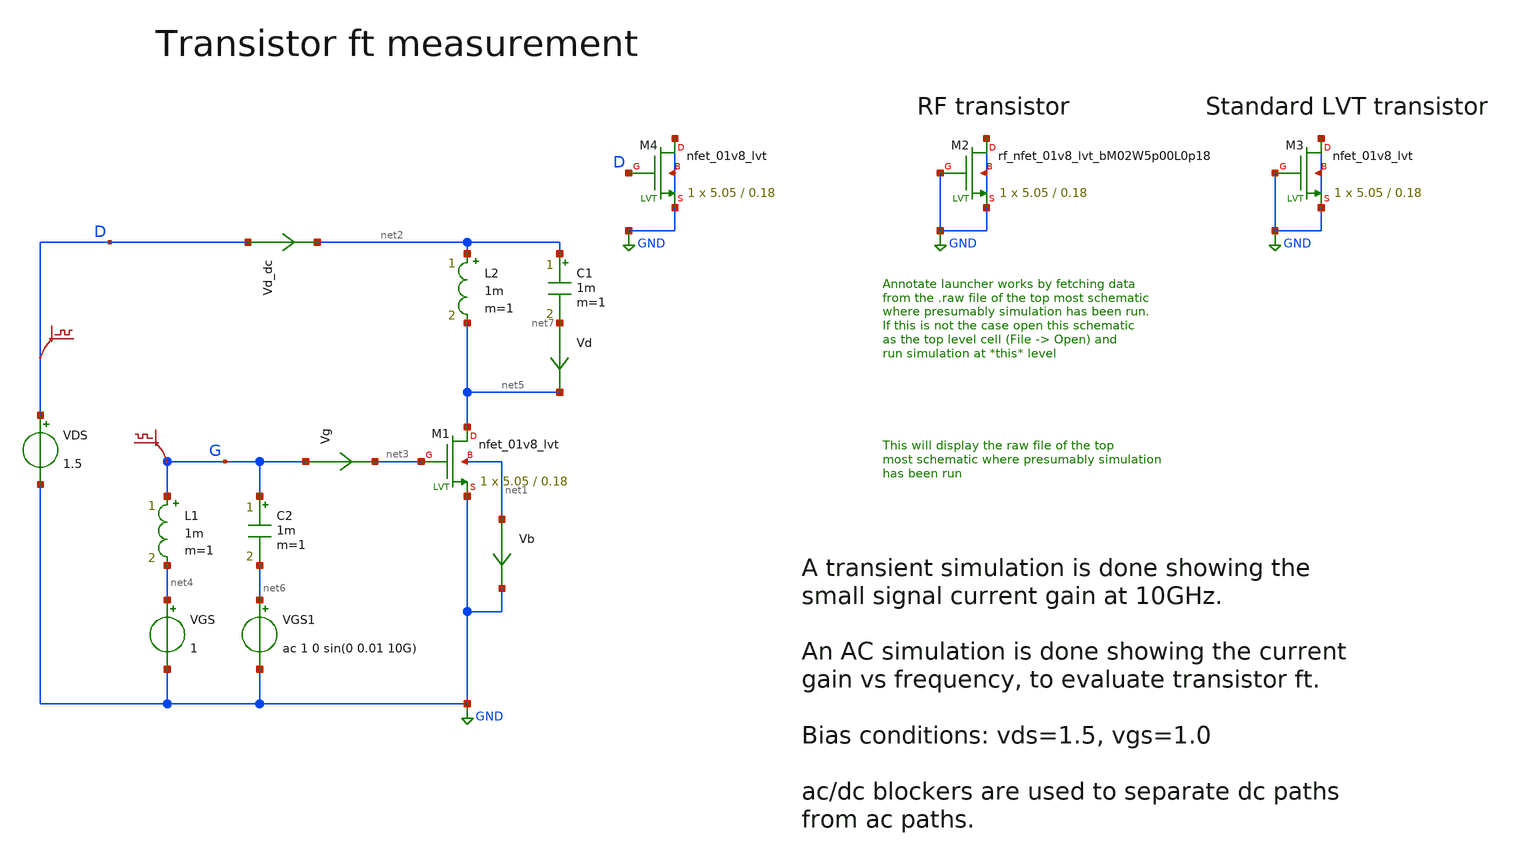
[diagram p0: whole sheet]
** sch_path: xyce/sky130A-xyce/libs.tech/xschem/sky130_tests/tb_ft_test_2.sch
**.subckt tb_ft_test_2
VDS D GND 1.5
VGS net4 GND 1
Vd net7 net5 0
.save i(vd)
L1 G net4 1m m=1
Vg G net3 0
.save i(vg)
L2 net2 net5 1m m=1
C1 net2 net7 1m m=1
C2 G net6 1m m=1
VGS1 net6 GND ac 1 0 sin(0 0.01 10G)
Vd_dc D net2 0
.save i(vd_dc)
.save v(g)
.save v(d)
Vb net1 GND 0
.save i(vb)
XM2 GND GND GND GND sky130_fd_pr__rf_nfet_01v8_lvt_bM02W5p00L0p18 L=0.18 W=5.05 nf=1 ad=0 as=0 pd=0
+ ps=0 nrd=0 nrs=0 sa=0 sb=0 sd=0 mult=1 m=1
XM3 GND GND GND GND sky130_fd_pr__nfet_01v8_lvt L=0.18 W=5.05 nf=1 ad='int((nf+1)/2) * W/nf * 0.29' as='int((nf+2)/2) * W/nf * 0.29'
+ pd='2*int((nf+1)/2) * (W/nf + 0.29)' ps='2*int((nf+2)/2) * (W/nf + 0.29)' nrd='0.29 / W' nrs='0.29 / W'
+ sa=0 sb=0 sd=0 mult=1 m=1
XM1 net5 net3 GND net1 sky130_fd_pr__nfet_01v8_lvt L=0.18 W=5.05 nf=1 ad='int((nf+1)/2) * W/nf * 0.29'
+ as='int((nf+2)/2) * W/nf * 0.29' pd='2*int((nf+1)/2) * (W/nf + 0.29)' ps='2*int((nf+2)/2) * (W/nf + 0.29)'
+ nrd='0.29 / W' nrs='0.29 / W' sa=0 sb=0 sd=0 mult=1 m=1
XM4 GND D GND GND sky130_fd_pr__nfet_01v8_lvt L=0.18 W=5.05 nf=1 ad='int((nf+1)/2) * W/nf * 0.29' as='int((nf+2)/2) * W/nf * 0.29'
+ pd='2*int((nf+1)/2) * (W/nf + 0.29)' ps='2*int((nf+2)/2) * (W/nf + 0.29)' nrd='0.29 / W' nrs='0.29 / W'
+ sa=0 sb=0 sd=0 mult=1 m=1
**** begin user architecture code

.include $::SKYWATER_MODELS/cells/nfet_01v8/sky130_fd_pr__nfet_01v8__tt.corner.spice
.include $::SKYWATER_MODELS/cells/nfet_01v8_lvt/sky130_fd_pr__nfet_01v8_lvt__tt.corner.spice
.include $::SKYWATER_MODELS/cells/pfet_01v8/sky130_fd_pr__pfet_01v8__tt.corner.spice
.include $::SKYWATER_MODELS/cells/nfet_03v3_nvt/sky130_fd_pr__nfet_03v3_nvt__tt.corner.spice
.include $::SKYWATER_MODELS/cells/nfet_05v0_nvt/sky130_fd_pr__nfet_05v0_nvt__tt.corner.spice
.include $::SKYWATER_MODELS/cells/esd_nfet_01v8/sky130_fd_pr__esd_nfet_01v8__tt.corner.spice
.include $::SKYWATER_MODELS/cells/pfet_01v8_lvt/sky130_fd_pr__pfet_01v8_lvt__tt.corner.spice
.include $::SKYWATER_MODELS/cells/pfet_01v8_hvt/sky130_fd_pr__pfet_01v8_hvt__tt.corner.spice
.include $::SKYWATER_MODELS/cells/esd_pfet_g5v0d10v5/sky130_fd_pr__esd_pfet_g5v0d10v5__tt.corner.spice
.include $::SKYWATER_MODELS/cells/pfet_g5v0d10v5/sky130_fd_pr__pfet_g5v0d10v5__tt.corner.spice
.include $::SKYWATER_MODELS/cells/pfet_g5v0d16v0/sky130_fd_pr__pfet_g5v0d16v0__tt.corner.spice
.include $::SKYWATER_MODELS/cells/nfet_g5v0d10v5/sky130_fd_pr__nfet_g5v0d10v5__tt.corner.spice
.include $::SKYWATER_MODELS/cells/nfet_g5v0d16v0/sky130_fd_pr__nfet_g5v0d16v0__tt_discrete.corner.spice
.include $::SKYWATER_MODELS/cells/esd_nfet_g5v0d10v5/sky130_fd_pr__esd_nfet_g5v0d10v5__tt.corner.spice
.include $::SKYWATER_MODELS/models/corners/tt/nonfet.spice
* Mismatch parameters
.include $::SKYWATER_MODELS/cells/nfet_01v8/sky130_fd_pr__nfet_01v8__mismatch.corner.spice
.include $::SKYWATER_MODELS/cells/pfet_01v8/sky130_fd_pr__pfet_01v8__mismatch.corner.spice
.include $::SKYWATER_MODELS/cells/nfet_01v8_lvt/sky130_fd_pr__nfet_01v8_lvt__mismatch.corner.spice
.include $::SKYWATER_MODELS/cells/pfet_01v8_lvt/sky130_fd_pr__pfet_01v8_lvt__mismatch.corner.spice
.include $::SKYWATER_MODELS/cells/pfet_01v8_hvt/sky130_fd_pr__pfet_01v8_hvt__mismatch.corner.spice
.include $::SKYWATER_MODELS/cells/nfet_g5v0d10v5/sky130_fd_pr__nfet_g5v0d10v5__mismatch.corner.spice
.include $::SKYWATER_MODELS/cells/pfet_g5v0d10v5/sky130_fd_pr__pfet_g5v0d10v5__mismatch.corner.spice
.include $::SKYWATER_MODELS/cells/nfet_05v0_nvt/sky130_fd_pr__nfet_05v0_nvt__mismatch.corner.spice
.include $::SKYWATER_MODELS/cells/nfet_03v3_nvt/sky130_fd_pr__nfet_03v3_nvt__mismatch.corner.spice
* Resistor$::SKYWATER_MODELS/Capacitor
.include $::SKYWATER_MODELS/models/r+c/res_typical__cap_typical.spice
.include $::SKYWATER_MODELS/models/r+c/res_typical__cap_typical__lin.spice
* Special cells
.include $::SKYWATER_MODELS/models/corners/tt/specialized_cells.spice
* All models
.include $::SKYWATER_MODELS/models/all.spice
* Corner
.include $::SKYWATER_MODELS/models/corners/tt/rf.spice



* this experimental option enables mos model bin
* selection based on W/NF instead of W
.option wnflag=1
.options method=gear savecurrents
.save all

.control
  save all
* save @m.xm1.msky130_fd_pr__rf_nfet_01v8_lvt_bm02w5p00l0p18[gm]
  save @m.xm1.msky130_fd_pr__nfet_01v8_lvt[gm]

  op
  write tb_ft_test_2.raw
  tran 0.001n 2n
  set appendwrite
  write tb_ft_test_2.raw
  ac dec 10 1000 1000G
  set appendwrite
  write tb_ft_test_2.raw

  setplot tran1
  plot i(vg) i(vd)

  setplot ac1
  plot db(i(vd)/i(vg))
.endc



**** end user architecture code
**.ends
.GLOBAL GND
.end
